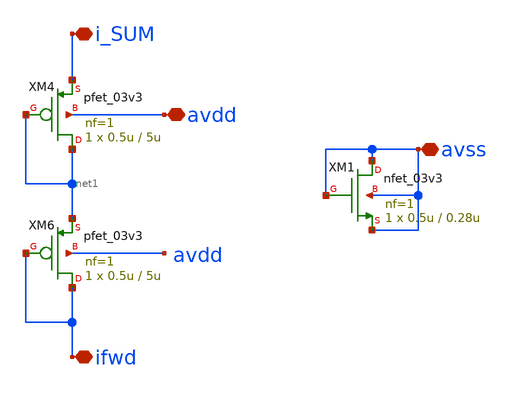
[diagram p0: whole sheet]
** sch_path: sch/Current_limit/Current-limit.sch
**.subckt Current-limit avdd ifwd i_SUM avss
*.iopin avdd
*.iopin ifwd
*.iopin i_SUM
*.iopin avss
XM4 net1 net1 i_SUM avdd pfet_03v3 L=5u W=0.5u nf=1 ad='int((nf+1)/2) * W/nf * 0.18u' as='int((nf+2)/2) * W/nf * 0.18u'
+ pd='2*int((nf+1)/2) * (W/nf + 0.18u)' ps='2*int((nf+2)/2) * (W/nf + 0.18u)' nrd='0.18u / W' nrs='0.18u / W'
+ sa=0 sb=0 sd=0 m=1
XM6 ifwd ifwd net1 avdd pfet_03v3 L=5u W=0.5u nf=1 ad='int((nf+1)/2) * W/nf * 0.18u' as='int((nf+2)/2) * W/nf * 0.18u'
+ pd='2*int((nf+1)/2) * (W/nf + 0.18u)' ps='2*int((nf+2)/2) * (W/nf + 0.18u)' nrd='0.18u / W' nrs='0.18u / W'
+ sa=0 sb=0 sd=0 m=1
XM1 avss avss avss avss nfet_03v3 L=0.28u W=0.5u nf=1 ad='int((nf+1)/2) * W/nf * 0.18u' as='int((nf+2)/2) * W/nf * 0.18u'
+ pd='2*int((nf+1)/2) * (W/nf + 0.18u)' ps='2*int((nf+2)/2) * (W/nf + 0.18u)' nrd='0.18u / W' nrs='0.18u / W'
+ sa=0 sb=0 sd=0 m=1
**.ends
.end
